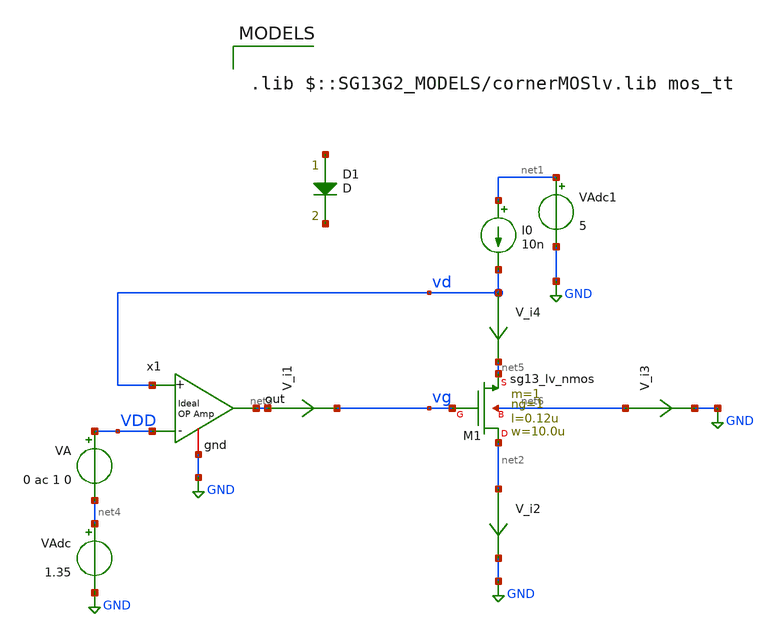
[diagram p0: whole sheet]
** sch_path: ihp_tutorials/nmos_ext_sigma.sch
**.subckt nmos_ext_sigma
x1 net3 vd VDD GND ampOp_ideal
I0 net1 vd 10n
VA VDD net4 0 ac 1 0
VAdc net4 GND 1.35
V_i2 net2 GND 0
.save i(v_i2)
XM1 net2 vg net5 net6 sg13_lv_nmos w=10.0u l=0.12u ng=1 m=1 mm_ok=1
VAdc1 net1 GND 5
V_i1 net3 vg 0
.save i(v_i1)
V_i3 net6 GND 0
.save i(v_i3)
V_i4 vd net5 0
.save i(v_i4)
D1 net7 net8 D area=1
**** begin user architecture code


.option savecurrents
.option gmin = 1e-24
.option retol = 1e-5

.ic V(vg) = 0.39

.control
  pre_osdi ./psp103_nqs.osdi
  save all
  op
  remzerovec
  write nmos_ext_sigma.raw
  set appendwrite

  *ac dec 100 1 1e10

  *remzerovec
  *write nmos_ext_sigma.raw

.endc
.save all



.lib $::SG13G2_MODELS/cornerMOSlv.lib mos_tt

**** end user architecture code
**.ends

* expanding   symbol:  /home/gmaranhao/Desktop/gf180_work/auxLib/ampOp_ideal.sym # of pins=4
** sym_path: gf_tutorials/auxLib/ampOp_ideal.sym
** sch_path: gf_tutorials/auxLib/ampOp_ideal.sch
.subckt ampOp_ideal out + - gnd
*.ipin +
*.ipin -
*.opin out
*.iopin gnd
E1 out gnd + - 10000000
.ends

.GLOBAL GND
.end
